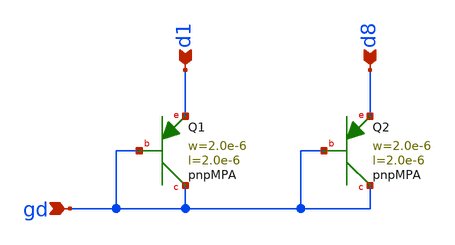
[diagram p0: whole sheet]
** sch_path: schematics/bandgap/bandgap_res_diodes.sch
**.subckt bandgap_res_diodes gd d1 d8
*.ipin gd
*.ipin d1
*.ipin d8
XQ1 gd gd d1 pnpMPA a=4p p=8u m=1
XQ2 gd gd d8 pnpMPA a=4p p=8u m=8
**.ends
.end
